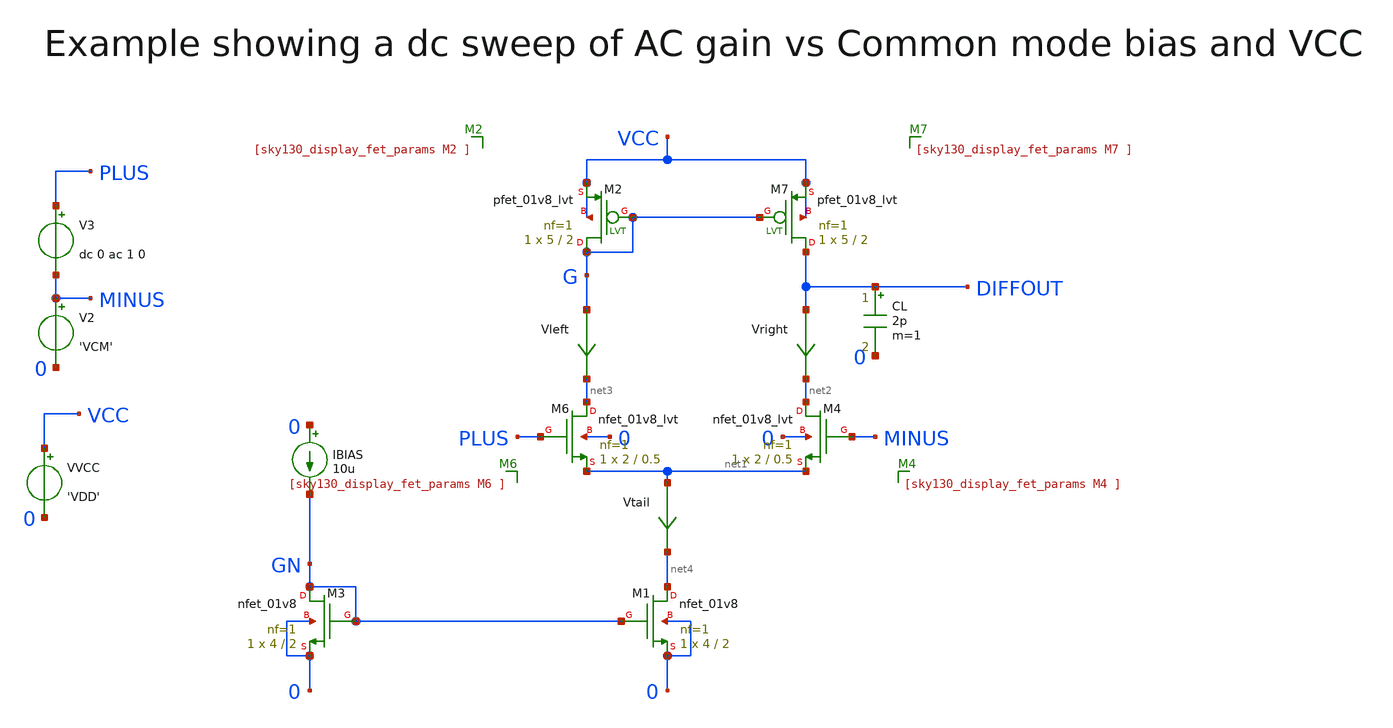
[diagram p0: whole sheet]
** sch_path: sky130A/xschem_libs/sky130_tests_ase/cmos_ac_sweep/schematic/cmos_ac_sweep.sch
* Copyright 2021 Stefan Frederik Schippers
* Licensed under the Apache License, Version 2.0 (the "License");
* you may not use this file except in compliance with the License.
* You may obtain a copy of the License at
* https://www.apache.org/licenses/LICENSE-2.0
* Unless required by applicable law or agreed to in writing, software
* distributed under the License is distributed on an "AS IS" BASIS,
* WITHOUT WARRANTIES OR CONDITIONS OF ANY KIND, either express or implied.
* See the License for the specific language governing permissions and
* limitations under the License.
**.subckt cmos_ac_sweep
VVCC VCC 0 'VDD'
IBIAS 0 GN 10u
CL DIFFOUT 0 2p m=1
Vright DIFFOUT net2 0
.save i(vright)
V3 PLUS MINUS dc 0 ac 1 0
V2 MINUS 0 'VCM'
XM7 DIFFOUT G VCC VCC sky130_fd_pr__pfet_01v8_lvt L=2 W=5 nf=1 ad='int((1 + 1)/2) * 5 / 1 * 0.29' as='int((1 + 2)/2) * 5 / 1 * 0.29'
+ pd='2*int((1 + 1)/2) * (5 / 1 + 0.29)' ps='2*int((1 + 2)/2) * (5 / 1 + 0.29)' nrd='0.29 / 5 ' nrs='0.29 / 5 '
+ sa=0 sb=0 sd=0 mult=1 m=1
XM2 G G VCC VCC sky130_fd_pr__pfet_01v8_lvt L=2 W=5 nf=1 ad='int((1 + 1)/2) * 5 / 1 * 0.29' as='int((1 + 2)/2) * 5 / 1 * 0.29'
+ pd='2*int((1 + 1)/2) * (5 / 1 + 0.29)' ps='2*int((1 + 2)/2) * (5 / 1 + 0.29)' nrd='0.29 / 5 ' nrs='0.29 / 5 '
+ sa=0 sb=0 sd=0 mult=1 m=1
XM6 net3 PLUS net1 0 sky130_fd_pr__nfet_01v8_lvt L=0.5 W=2 nf=1 ad='int((1 + 1)/2) * 2 / 1 * 0.29' as='int((1 + 2)/2) * 2 / 1 * 0.29'
+ pd='2*int((1 + 1)/2) * (2 / 1 + 0.29)' ps='2*int((1 + 2)/2) * (2 / 1 + 0.29)' nrd='0.29 / 2 ' nrs='0.29 / 2 '
+ sa=0 sb=0 sd=0 mult=1 m=1
XM4 net2 MINUS net1 0 sky130_fd_pr__nfet_01v8_lvt L=0.5 W=2 nf=1 ad='int((1 + 1)/2) * 2 / 1 * 0.29' as='int((1 + 2)/2) * 2 / 1 * 0.29'
+ pd='2*int((1 + 1)/2) * (2 / 1 + 0.29)' ps='2*int((1 + 2)/2) * (2 / 1 + 0.29)' nrd='0.29 / 2 ' nrs='0.29 / 2 '
+ sa=0 sb=0 sd=0 mult=1 m=1
XM1 net4 GN 0 0 sky130_fd_pr__nfet_01v8 L=2 W=4 nf=1 ad='int((1 + 1)/2) * 4 / 1 * 0.29' as='int((1 + 2)/2) * 4 / 1 * 0.29'
+ pd='2*int((1 + 1)/2) * (4 / 1 + 0.29)' ps='2*int((1 + 2)/2) * (4 / 1 + 0.29)' nrd='0.29 / 4 ' nrs='0.29 / 4 '
+ sa=0 sb=0 sd=0 mult=1 m=1
XM3 GN GN 0 0 sky130_fd_pr__nfet_01v8 L=2 W=4 nf=1 ad='int((1 + 1)/2) * 4 / 1 * 0.29' as='int((1 + 2)/2) * 4 / 1 * 0.29'
+ pd='2*int((1 + 1)/2) * (4 / 1 + 0.29)' ps='2*int((1 + 2)/2) * (4 / 1 + 0.29)' nrd='0.29 / 4 ' nrs='0.29 / 4 '
+ sa=0 sb=0 sd=0 mult=1 m=1
Vtail net1 net4 0
.save i(vtail)
Vleft G net3 0
.save i(vleft)
**.ends
.end
